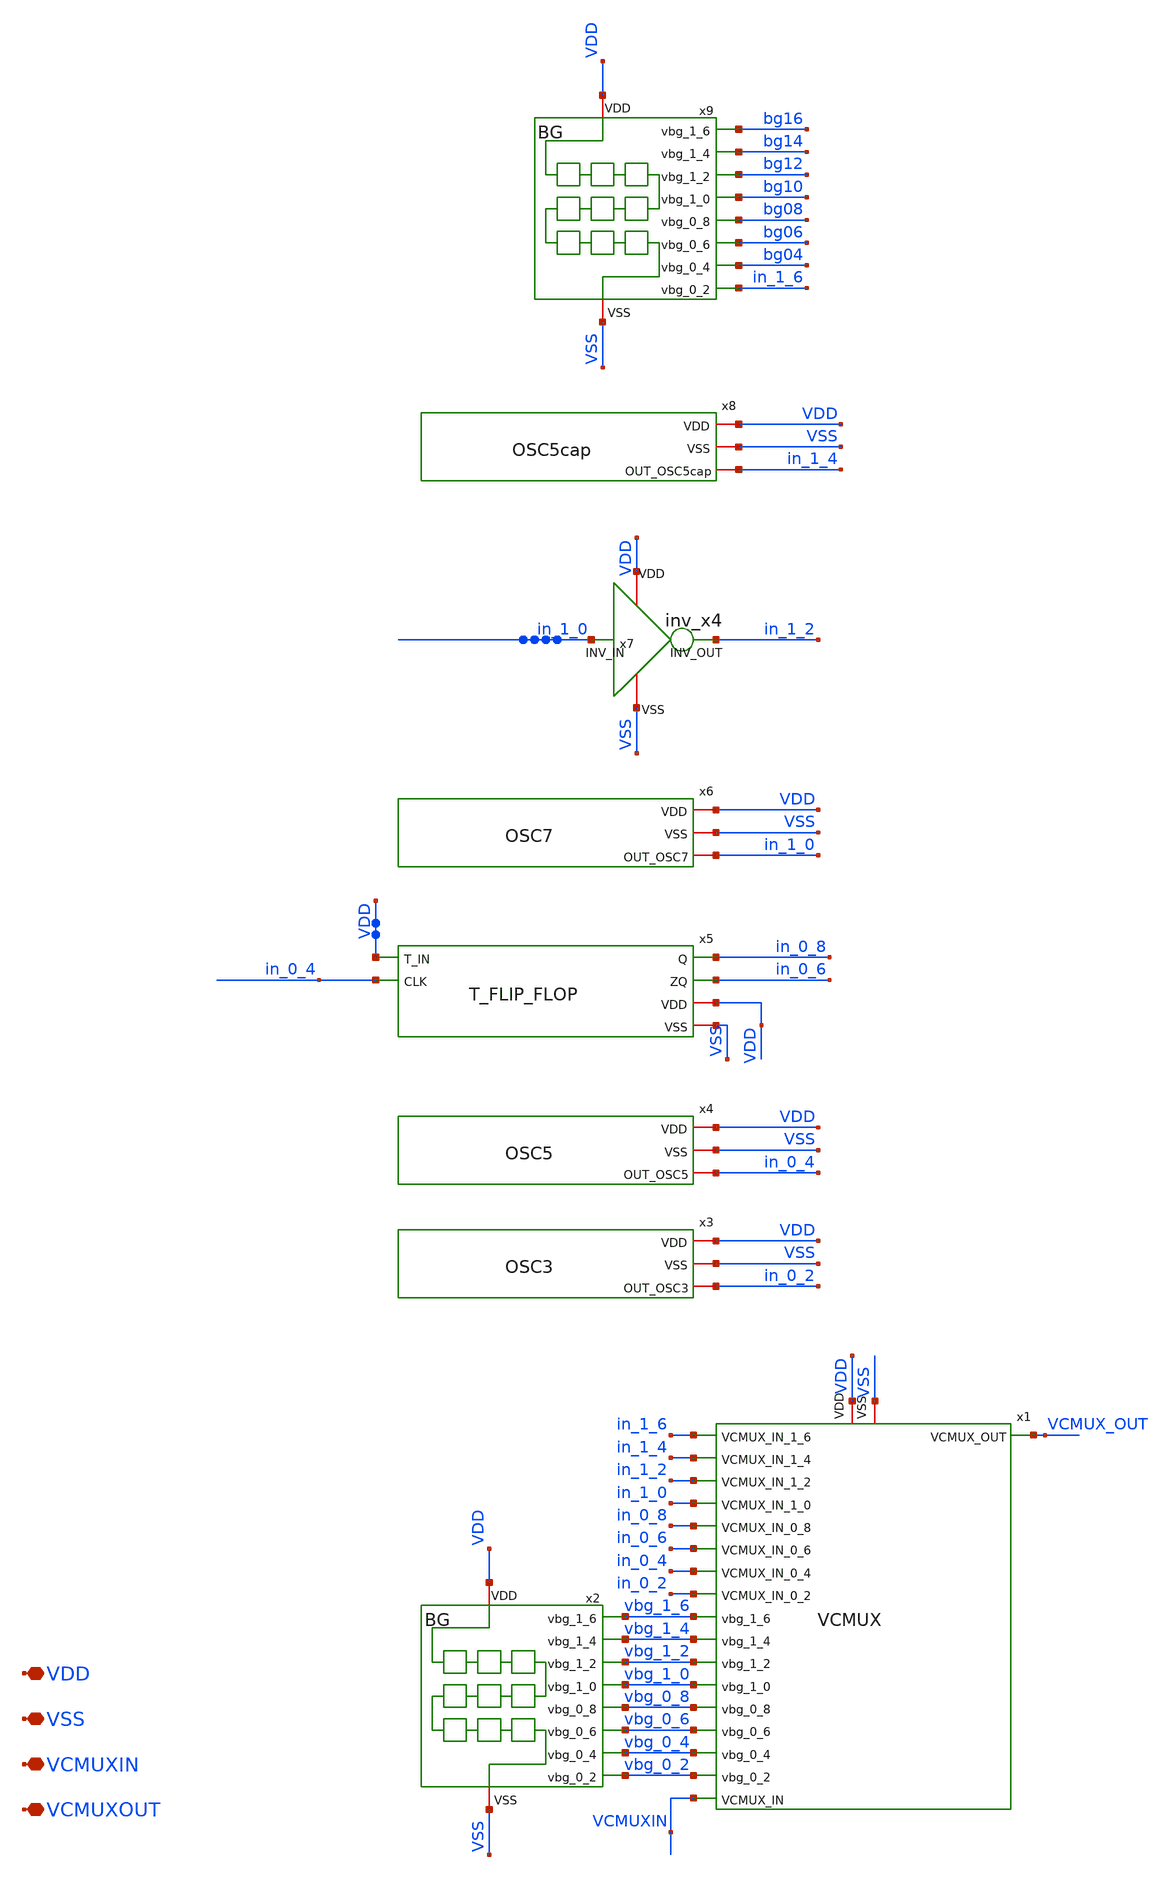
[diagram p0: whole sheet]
** sch_path: xschem/untitled-6.sch
**.subckt untitled-6 VDD VSS VCMUXIN VCMUXOUT
*.iopin VDD
*.iopin VSS
*.iopin VCMUXIN
*.iopin VCMUXOUT
x2 vbg_1_6 vbg_1_4 vbg_1_2 vbg_1_0 vbg_0_8 vbg_0_6 vbg_0_4 vbg_0_2 VDD VSS BG
x1 in_1_6 VCMUX_OUT in_1_4 in_1_2 in_1_0 in_0_8 in_0_6 in_0_4 in_0_2 vbg_1_6 VDD vbg_1_4 VSS vbg_1_2
+ vbg_1_0 vbg_0_8 vbg_0_6 vbg_0_4 vbg_0_2 VCMUXIN VCMUX
x5 in_0_8 VDD in_0_4 in_0_6 VDD VSS T_FLIP_FLOP
x7 VDD VSS in_1_2 in_1_0 inv_x4
x9 bg16 bg14 bg12 bg10 bg08 bg06 bg04 in_1_6 VDD VSS BG
x3 VDD VSS in_0_2 OSC3
x4 VDD VSS in_0_4 OSC5
x6 VDD VSS in_1_0 OSC7
x8 VDD VSS in_1_4 OSC5cap
**.ends
.end
